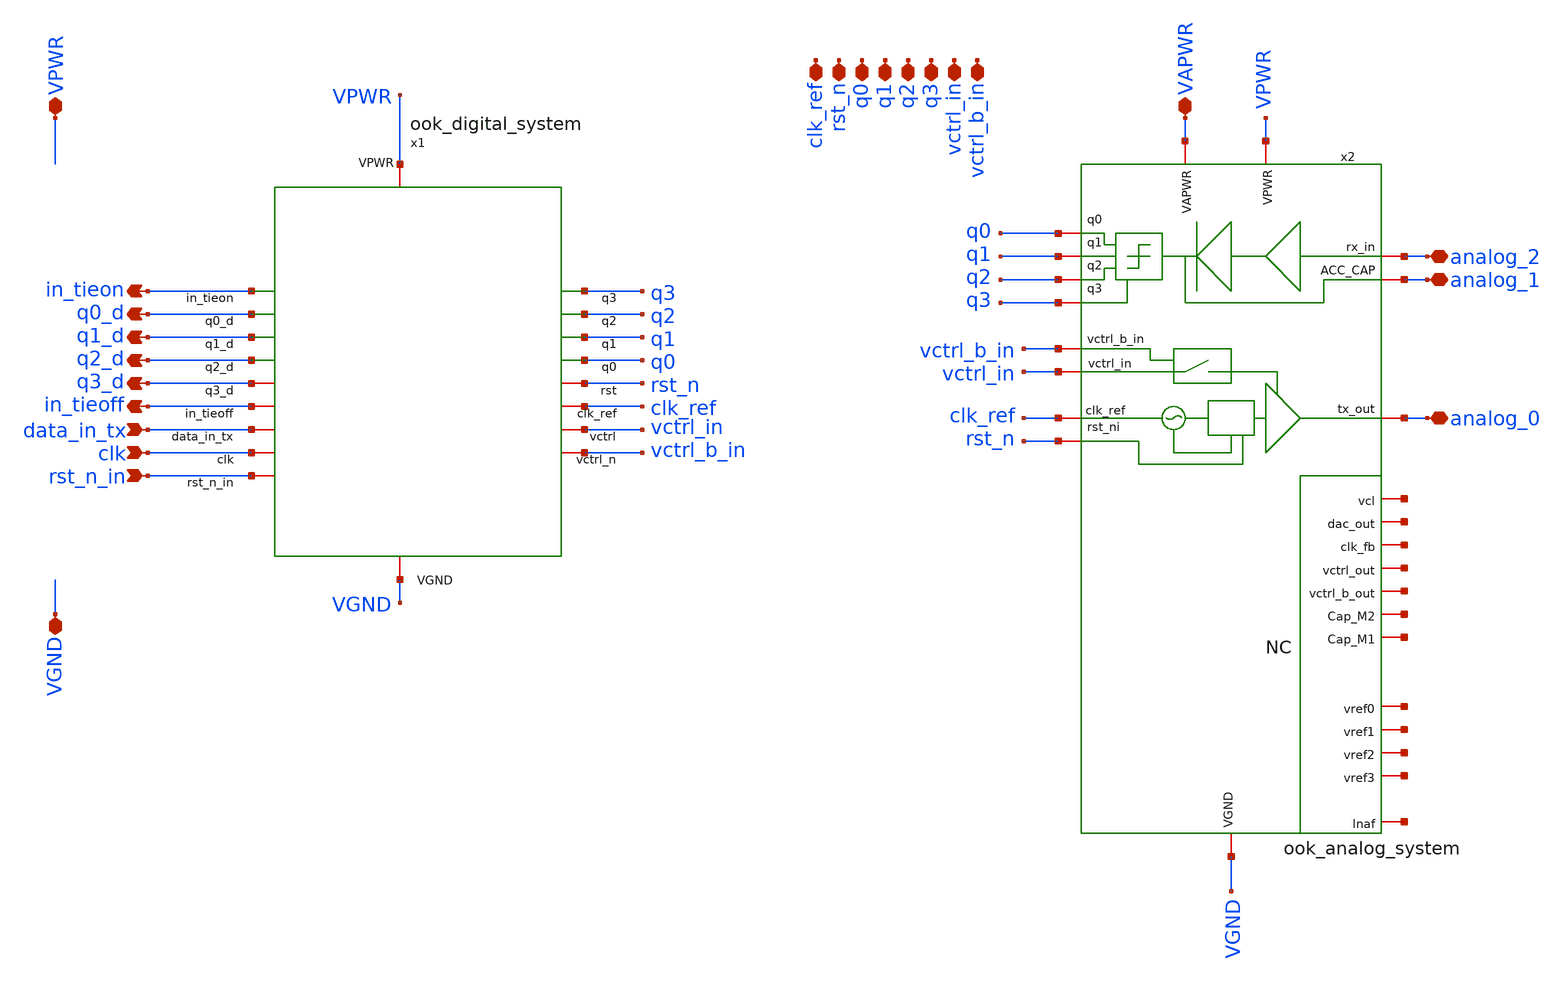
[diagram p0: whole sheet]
** sch_path: macros/heichips26_ook_top/schematic/xschem/heichips26_ook_soc.sch
**.subckt heichips26_ook_soc VPWR VGND VAPWR analog_2 analog_1 analog_0 q0 q1 q2 q3 vctrl_in
*+ vctrl_b_in rst_n clk_ref in_tieon q0_d q1_d q2_d q3_d in_tieoff data_in_tx clk rst_n_in
*.iopin VPWR
*.iopin VGND
*.iopin VAPWR
*.iopin analog_2
*.iopin analog_1
*.iopin analog_0
*.iopin q0
*.iopin q1
*.iopin q2
*.iopin q3
*.iopin vctrl_in
*.iopin vctrl_b_in
*.iopin rst_n
*.iopin clk_ref
*.opin in_tieon
*.opin q0_d
*.opin q1_d
*.opin q2_d
*.opin q3_d
*.opin in_tieoff
*.ipin data_in_tx
*.ipin clk
*.ipin rst_n_in
x2 VAPWR net1 VPWR q3 q2 analog_0 analog_2 q1 q0 vctrl_in net2 vctrl_b_in net3 analog_1 net4 net5
+ net6 clk_ref net7 net8 rst_n net9 VGND net10 net11 net12 ook_analog_system
x1 VGND VPWR clk clk_ref data_in_tx in_tieoff in_tieon q0 q0_d q1 q1_d q2 q2_d q3 q3_d rst_n
+ rst_n_in vctrl_in vctrl_b_in ook_digital_system
**.ends
.end
